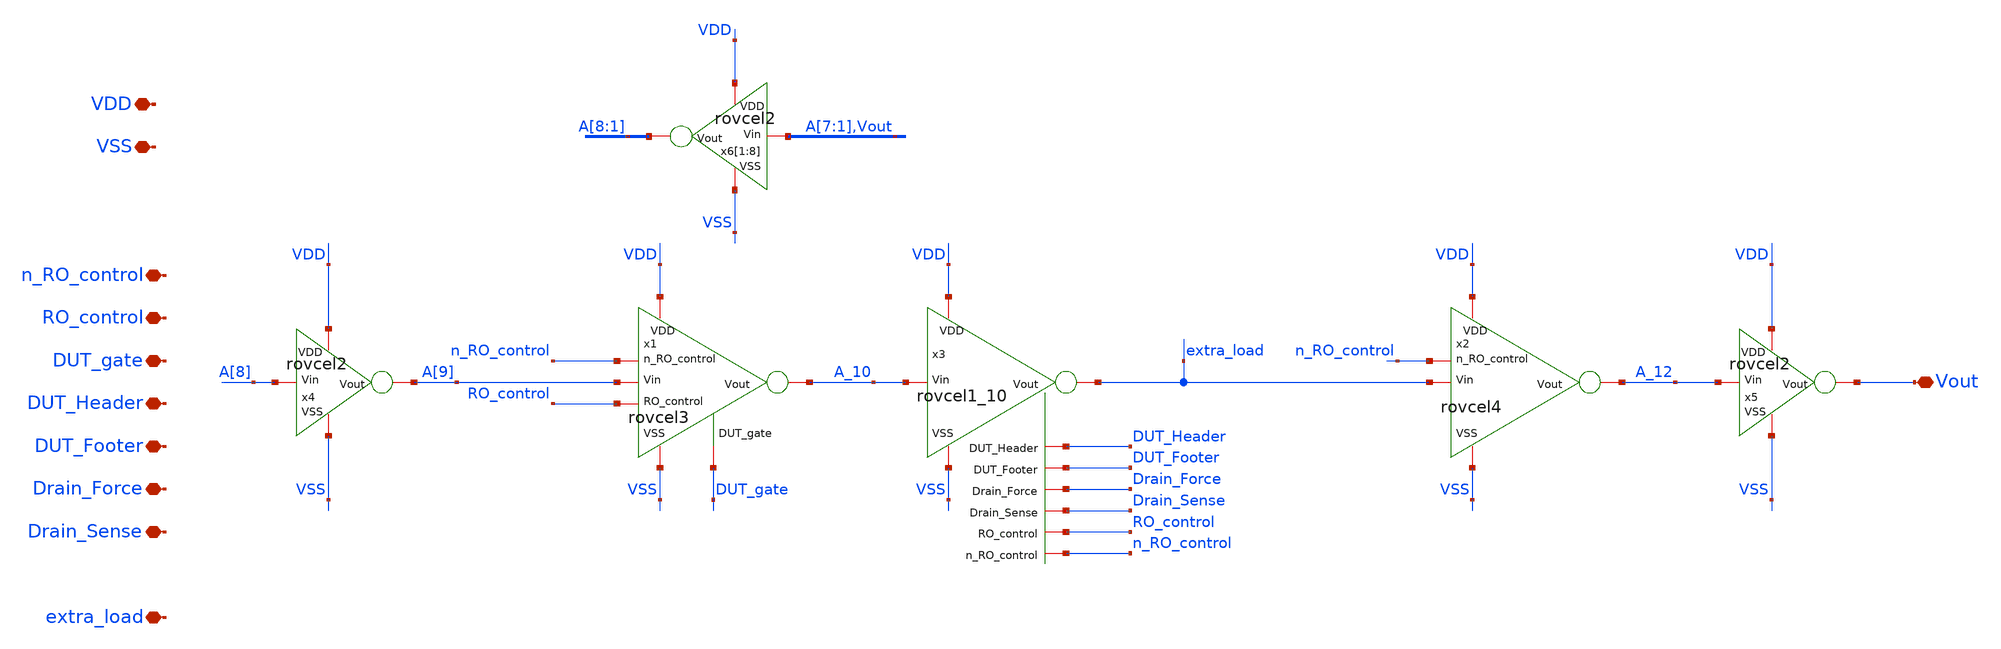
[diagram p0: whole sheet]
** sch_path: unic_cass_wrapper_user_project/ROs_reliability/top_RO_core_13_10x.sch
**.subckt top_RO_core_13_10x VDD VSS n_RO_control RO_control DUT_gate extra_load DUT_Header
*+ DUT_Footer Drain_Force Drain_Sense Vout
*.iopin VDD
*.iopin VSS
*.iopin n_RO_control
*.iopin RO_control
*.iopin DUT_gate
*.iopin extra_load
*.iopin DUT_Header
*.iopin DUT_Footer
*.iopin Drain_Force
*.iopin Drain_Sense
*.iopin Vout
x4 VDD VSS A[9] A[8] rovcel2
x3 DUT_Header DUT_Footer Drain_Force Drain_Sense RO_control n_RO_control VDD VSS A_10 extra_load
+ rovcel1_10
x1 VDD VSS A[9] n_RO_control A_10 RO_control DUT_gate rovcel3
x2 VDD VSS extra_load n_RO_control A_12 rovcel4
x5 VDD VSS Vout A_12 rovcel2
x6[1] VDD VSS A[8] A[7] rovcel2
x6[2] VDD VSS A[7] A[6] rovcel2
x6[3] VDD VSS A[6] A[5] rovcel2
x6[4] VDD VSS A[5] A[4] rovcel2
x6[5] VDD VSS A[4] A[3] rovcel2
x6[6] VDD VSS A[3] A[2] rovcel2
x6[7] VDD VSS A[2] A[1] rovcel2
x6[8] VDD VSS A[1] Vout rovcel2
**.ends

* expanding   symbol:  rovcel2.sym # of pins=4
** sym_path: rovcel2.sym
** sch_path: rovcel2.sch
.subckt rovcel2 VDD VSS Vout Vin
*.iopin VDD
*.iopin VSS
*.iopin Vin
*.iopin Vout
* noconn #net1
* noconn #net2
x5 VDD Vin Vout VSS inverter_RO_rel
x1 VDD VDD Vout net2 VSS VSS tgate
x3 VDD VDD Vout net1 VSS VSS tgate
.ends


* expanding   symbol:  rovcel1_10.sym # of pins=10
** sym_path: rovcel1_10.sym
** sch_path: rovcel1_10.sch
.subckt rovcel1_10 DUT_Header DUT_Footer Drain_Force Drain_Sense RO_control n_RO_control VDD VSS Vin
+ Vout
*.iopin VDD
*.iopin VSS
*.iopin Vin
*.iopin DUT_Header
*.iopin DUT_Footer
*.iopin Drain_Force
*.iopin Vout
*.iopin Drain_Sense
*.iopin RO_control
*.iopin n_RO_control
x1 VDD VSS Vin DUT_Header DUT_Footer Vout tristate_inv
x2 RO_control VDD Vout Drain_Sense VSS n_RO_control tgate
x3 RO_control VDD Vout Drain_Force VSS n_RO_control tgate_force10
.ends


* expanding   symbol:  rovcel3.sym # of pins=7
** sym_path: rovcel3.sym
** sch_path: rovcel3.sch
.subckt rovcel3 VDD VSS Vin n_RO_control Vout RO_control DUT_gate
*.iopin VDD
*.iopin VSS
*.iopin Vin
*.iopin n_RO_control
*.iopin RO_control
*.iopin DUT_gate
*.iopin Vout
* noconn #net1
x4 VDD VSS Vin n_RO_control RO_control Vout tristate_inv
x1 RO_control VDD Vout net1 VSS n_RO_control tgate
x5 RO_control VDD Vout DUT_gate VSS n_RO_control tgate
.ends


* expanding   symbol:  rovcel4.sym # of pins=5
** sym_path: rovcel4.sym
** sch_path: rovcel4.sch
.subckt rovcel4 VDD VSS Vin n_RO_control Vout
*.iopin VDD
*.iopin VSS
*.iopin Vin
*.iopin n_RO_control
*.iopin Vout
* noconn #net1
x4 n_RO_control VDD VSS Vin Vout inv1
x1 VDD VDD Vout VSS VSS VSS tgate
x5 VDD VDD Vout net1 VSS VSS tgate
.ends


* expanding   symbol:  inverter_RO_rel.sym # of pins=4
** sym_path: inverter_RO_rel.sym
** sch_path: inverter_RO_rel.sch
.subckt inverter_RO_rel VDD Vin Vout VSS
*.iopin VDD
*.iopin VSS
*.iopin Vin
*.iopin Vout
XM3 Vout Vin VDD VDD sg13_lv_pmos w=3.4u l=0.45u ng=1 m=4 mm_ok=1
XM1 VSS Vin Vout VSS sg13_lv_nmos w=1.3u l=0.45u ng=1 m=4 mm_ok=1
.ends


* expanding   symbol:  tgate.sym # of pins=6
** sym_path: tgate.sym
** sch_path: tgate.sch
.subckt tgate nclk VDD Vin Vout VSS clk
*.iopin nclk
*.iopin clk
*.iopin VDD
*.iopin VSS
*.iopin Vout
*.iopin Vin
XM3 Vout nclk Vin VDD sg13_lv_pmos w=3.4u l=0.45u ng=1 m=1 mm_ok=1
XM1 Vout clk Vin VSS sg13_lv_nmos w=1.3u l=0.45u ng=1 m=1 mm_ok=1
.ends


* expanding   symbol:  tristate_inv.sym # of pins=6
** sym_path: tristate_inv.sym
** sch_path: tristate_inv.sch
.subckt tristate_inv VDD VSS Vin Vup Vdn Vout
*.iopin VDD
*.iopin VSS
*.iopin Vin
*.iopin Vout
*.iopin Vup
*.iopin Vdn
XM5 Vout Vin net1 VDD sg13_lv_pmos w=3.4u l=0.45u ng=1 m=4 mm_ok=1
XM2 net2 Vin Vout VSS sg13_lv_nmos w=1.3u l=0.45u ng=1 m=4 mm_ok=1
XM1 net1 Vup VDD VDD sg13_lv_pmos w=3.4u l=0.45u ng=1 m=12 mm_ok=1
XM3 VSS Vdn net2 VSS sg13_lv_nmos w=1.3u l=0.45u ng=1 m=12 mm_ok=1
.ends


* expanding   symbol:  tgate_force10.sym # of pins=6
** sym_path: tgate_force10.sym
** sch_path: tgate_force10.sch
.subckt tgate_force10 nclk VDD Vin Vout VSS clk
*.iopin nclk
*.iopin clk
*.iopin VDD
*.iopin VSS
*.iopin Vout
*.iopin Vin
XM1 Vout nclk Vin VDD sg13_lv_pmos w=3.4u l=0.45u ng=1 m=12 mm_ok=1
XM3 Vout clk Vin VSS sg13_lv_nmos w=1.3u l=0.45u ng=1 m=12 mm_ok=1
.ends


* expanding   symbol:  inv1.sym # of pins=5
** sym_path: inv1.sym
** sch_path: inv1.sch
.subckt inv1 n_RO_control VDD VSS Vin Vout
*.iopin VDD
*.iopin VSS
*.iopin Vin
*.iopin Vout
*.iopin n_RO_control
XM1 net1 n_RO_control VDD VDD sg13_lv_pmos w=3.4u l=0.45u ng=1 m=12 mm_ok=1
XM5 Vout Vin net1 VDD sg13_lv_pmos w=3.4u l=0.45u ng=1 m=4 mm_ok=1
XM2 VSS Vin Vout VSS sg13_lv_nmos w=1.3u l=0.45u ng=1 m=4 mm_ok=1
.ends

.end
